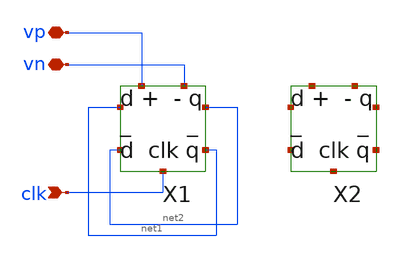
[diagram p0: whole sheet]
** sch_path: xschem/logic_gates/untitled.sch
**.subckt untitled vp vn clk
*.iopin vp
*.iopin vn
*.ipin clk
X1 net1 net2 net1 net2 clk vp vn dflipflop
X2 net3 net4 net5 net6 net7 net8 net9 dflipflop
**.ends

* expanding   symbol:  /home/madvlsi/dev/git/magic-dds/xschem/logic_gates/dflipflop.sym # of pins=7
** sym_path: xschem/logic_gates/dflipflop.sym
** sch_path: xschem/logic_gates/dflipflop.sch
.subckt dflipflop q_bar q d d_bar clk vp vn
*.opin q
*.opin q_bar
*.iopin vp
*.iopin vn
*.ipin d_bar
*.ipin d
*.ipin clk
XM8 vp net2 net3 vp sky130_fd_pr__pfet_01v8 L=0.15 W=1 nf=1 ad='int((nf+1)/2) * W/nf * 0.29' as='int((nf+2)/2) * W/nf * 0.29'
+ pd='2*int((nf+1)/2) * (W/nf + 0.29)' ps='2*int((nf+2)/2) * (W/nf + 0.29)' nrd='0.29 / W' nrs='0.29 / W'
+ sa=0 sb=0 sd=0 mult=1 m=1
XM9 vp net3 net2 vp sky130_fd_pr__pfet_01v8 L=0.15 W=1 nf=1 ad='int((nf+1)/2) * W/nf * 0.29' as='int((nf+2)/2) * W/nf * 0.29'
+ pd='2*int((nf+1)/2) * (W/nf + 0.29)' ps='2*int((nf+2)/2) * (W/nf + 0.29)' nrd='0.29 / W' nrs='0.29 / W'
+ sa=0 sb=0 sd=0 mult=1 m=1
XM5 net4 clk vn vn sky130_fd_pr__nfet_01v8 L=0.15 W=1 nf=1 ad='int((nf+1)/2) * W/nf * 0.29' as='int((nf+2)/2) * W/nf * 0.29'
+ pd='2*int((nf+1)/2) * (W/nf + 0.29)' ps='2*int((nf+2)/2) * (W/nf + 0.29)' nrd='0.29 / W' nrs='0.29 / W'
+ sa=0 sb=0 sd=0 mult=1 m=1
XM6 net3 net2 net4 vn sky130_fd_pr__nfet_01v8 L=0.15 W=1 nf=1 ad='int((nf+1)/2) * W/nf * 0.29' as='int((nf+2)/2) * W/nf * 0.29'
+ pd='2*int((nf+1)/2) * (W/nf + 0.29)' ps='2*int((nf+2)/2) * (W/nf + 0.29)' nrd='0.29 / W' nrs='0.29 / W'
+ sa=0 sb=0 sd=0 mult=1 m=1
XM7 net2 net3 net4 vn sky130_fd_pr__nfet_01v8 L=0.15 W=1 nf=1 ad='int((nf+1)/2) * W/nf * 0.29' as='int((nf+2)/2) * W/nf * 0.29'
+ pd='2*int((nf+1)/2) * (W/nf + 0.29)' ps='2*int((nf+2)/2) * (W/nf + 0.29)' nrd='0.29 / W' nrs='0.29 / W'
+ sa=0 sb=0 sd=0 mult=1 m=1
XM13 vn q q_bar vn sky130_fd_pr__nfet_01v8 L=0.15 W=1 nf=1 ad='int((nf+1)/2) * W/nf * 0.29' as='int((nf+2)/2) * W/nf * 0.29'
+ pd='2*int((nf+1)/2) * (W/nf + 0.29)' ps='2*int((nf+2)/2) * (W/nf + 0.29)' nrd='0.29 / W' nrs='0.29 / W'
+ sa=0 sb=0 sd=0 mult=1 m=1
XM3 q clk net2 vn sky130_fd_pr__nfet_01v8 L=0.30 W=1 nf=1 ad='int((nf+1)/2) * W/nf * 0.29' as='int((nf+2)/2) * W/nf * 0.29'
+ pd='2*int((nf+1)/2) * (W/nf + 0.29)' ps='2*int((nf+2)/2) * (W/nf + 0.29)' nrd='0.29 / W' nrs='0.29 / W'
+ sa=0 sb=0 sd=0 mult=1 m=1
XM4 q_bar clk net3 vn sky130_fd_pr__nfet_01v8 L=0.30 W=1 nf=1 ad='int((nf+1)/2) * W/nf * 0.29' as='int((nf+2)/2) * W/nf * 0.29'
+ pd='2*int((nf+1)/2) * (W/nf + 0.29)' ps='2*int((nf+2)/2) * (W/nf + 0.29)' nrd='0.29 / W' nrs='0.29 / W'
+ sa=0 sb=0 sd=0 mult=1 m=1
XM14 vn q_bar q vn sky130_fd_pr__nfet_01v8 L=0.15 W=1 nf=1 ad='int((nf+1)/2) * W/nf * 0.29' as='int((nf+2)/2) * W/nf * 0.29'
+ pd='2*int((nf+1)/2) * (W/nf + 0.29)' ps='2*int((nf+2)/2) * (W/nf + 0.29)' nrd='0.29 / W' nrs='0.29 / W'
+ sa=0 sb=0 sd=0 mult=1 m=1
XM10 net1 clk vp vp sky130_fd_pr__pfet_01v8 L=0.15 W=1 nf=1 ad='int((nf+1)/2) * W/nf * 0.29' as='int((nf+2)/2) * W/nf * 0.29'
+ pd='2*int((nf+1)/2) * (W/nf + 0.29)' ps='2*int((nf+2)/2) * (W/nf + 0.29)' nrd='0.29 / W' nrs='0.29 / W'
+ sa=0 sb=0 sd=0 mult=1 m=1
XM11 q_bar q net1 vp sky130_fd_pr__pfet_01v8 L=0.15 W=1 nf=1 ad='int((nf+1)/2) * W/nf * 0.29' as='int((nf+2)/2) * W/nf * 0.29'
+ pd='2*int((nf+1)/2) * (W/nf + 0.29)' ps='2*int((nf+2)/2) * (W/nf + 0.29)' nrd='0.29 / W' nrs='0.29 / W'
+ sa=0 sb=0 sd=0 mult=1 m=1
XM12 q q_bar net1 vp sky130_fd_pr__pfet_01v8 L=0.15 W=1 nf=1 ad='int((nf+1)/2) * W/nf * 0.29' as='int((nf+2)/2) * W/nf * 0.29'
+ pd='2*int((nf+1)/2) * (W/nf + 0.29)' ps='2*int((nf+2)/2) * (W/nf + 0.29)' nrd='0.29 / W' nrs='0.29 / W'
+ sa=0 sb=0 sd=0 mult=1 m=1
XM15 net4 clk vn vn sky130_fd_pr__nfet_01v8 L=0.15 W=1 nf=1 ad='int((nf+1)/2) * W/nf * 0.29' as='int((nf+2)/2) * W/nf * 0.29'
+ pd='2*int((nf+1)/2) * (W/nf + 0.29)' ps='2*int((nf+2)/2) * (W/nf + 0.29)' nrd='0.29 / W' nrs='0.29 / W'
+ sa=0 sb=0 sd=0 mult=1 m=1
XM16 net1 clk vp vp sky130_fd_pr__pfet_01v8 L=0.15 W=1 nf=1 ad='int((nf+1)/2) * W/nf * 0.29' as='int((nf+2)/2) * W/nf * 0.29'
+ pd='2*int((nf+1)/2) * (W/nf + 0.29)' ps='2*int((nf+2)/2) * (W/nf + 0.29)' nrd='0.29 / W' nrs='0.29 / W'
+ sa=0 sb=0 sd=0 mult=1 m=1
XM1 net2 clk d vp sky130_fd_pr__pfet_01v8 L=0.30 W=1 nf=1 ad='int((nf+1)/2) * W/nf * 0.29' as='int((nf+2)/2) * W/nf * 0.29'
+ pd='2*int((nf+1)/2) * (W/nf + 0.29)' ps='2*int((nf+2)/2) * (W/nf + 0.29)' nrd='0.29 / W' nrs='0.29 / W'
+ sa=0 sb=0 sd=0 mult=1 m=1
XM2 net3 clk d_bar vp sky130_fd_pr__pfet_01v8 L=0.30 W=1 nf=1 ad='int((nf+1)/2) * W/nf * 0.29' as='int((nf+2)/2) * W/nf * 0.29'
+ pd='2*int((nf+1)/2) * (W/nf + 0.29)' ps='2*int((nf+2)/2) * (W/nf + 0.29)' nrd='0.29 / W' nrs='0.29 / W'
+ sa=0 sb=0 sd=0 mult=1 m=1
.ends

.end
